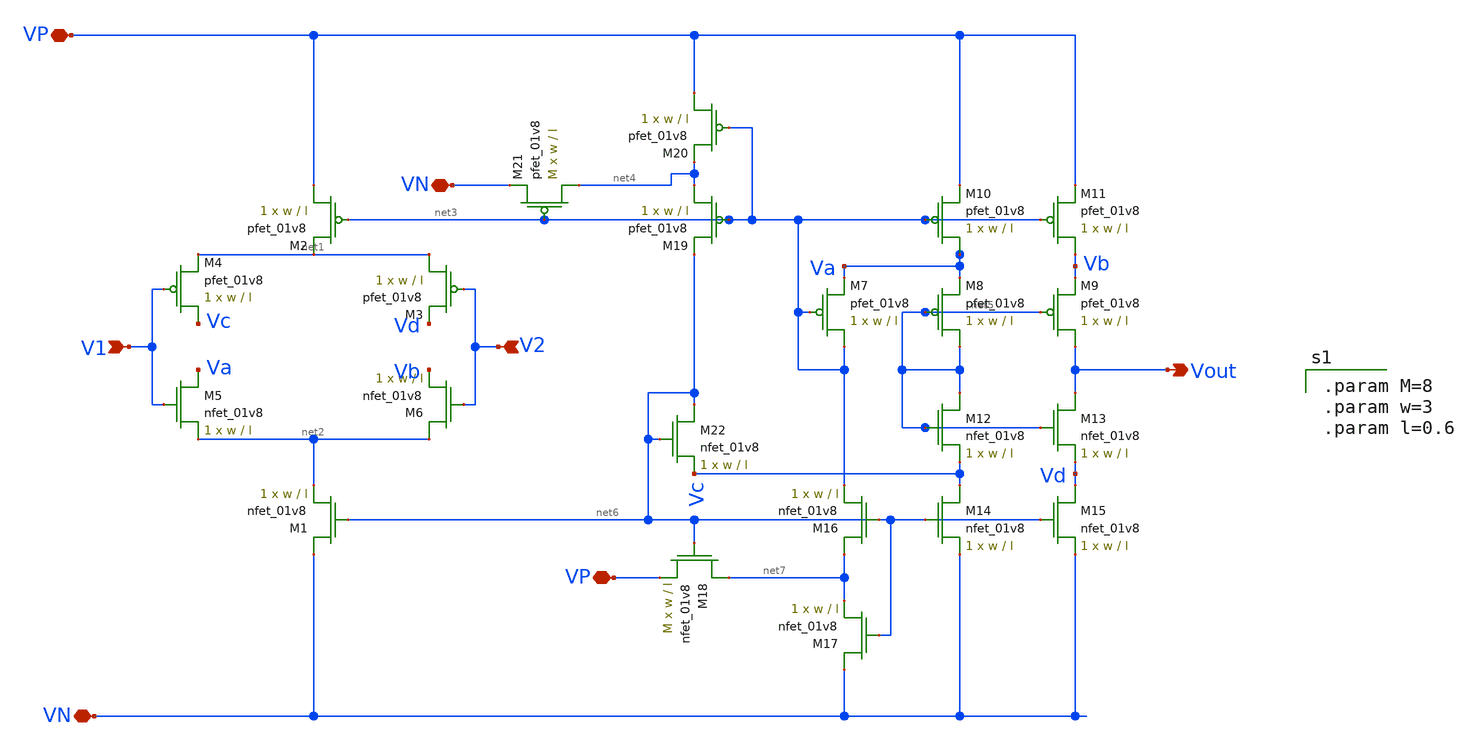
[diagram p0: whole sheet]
** sch_path: schematics/opamp.sch
**.subckt opamp V1 V2 Vout VP VN VP VN
*.ipin V1
*.ipin V2
*.opin Vout
*.iopin VP
*.iopin VN
*.iopin VP
*.iopin VN
XM1 VN net6 net2 GND sky130_fd_pr__nfet_01v8 L=l W=w nf=1 ad='int((nf+1)/2) * W/nf * 0.29' as='int((nf+2)/2) * W/nf * 0.29'
+ pd='2*int((nf+1)/2) * (W/nf + 0.29)' ps='2*int((nf+2)/2) * (W/nf + 0.29)' nrd='0.29 / W' nrs='0.29 / W'
+ sa=0 sb=0 sd=0 mult=1 m=1
XM2 VP net3 net1 VDD sky130_fd_pr__pfet_01v8 L=l W=w nf=1 ad='int((nf+1)/2) * W/nf * 0.29' as='int((nf+2)/2) * W/nf * 0.29'
+ pd='2*int((nf+1)/2) * (W/nf + 0.29)' ps='2*int((nf+2)/2) * (W/nf + 0.29)' nrd='0.29 / W' nrs='0.29 / W'
+ sa=0 sb=0 sd=0 mult=1 m=1
XM3 net1 V2 Vd VDD sky130_fd_pr__pfet_01v8 L=l W=w nf=1 ad='int((nf+1)/2) * W/nf * 0.29' as='int((nf+2)/2) * W/nf * 0.29'
+ pd='2*int((nf+1)/2) * (W/nf + 0.29)' ps='2*int((nf+2)/2) * (W/nf + 0.29)' nrd='0.29 / W' nrs='0.29 / W'
+ sa=0 sb=0 sd=0 mult=1 m=1
XM4 Vc V1 net1 VDD sky130_fd_pr__pfet_01v8 L=l W=w nf=1 ad='int((nf+1)/2) * W/nf * 0.29' as='int((nf+2)/2) * W/nf * 0.29'
+ pd='2*int((nf+1)/2) * (W/nf + 0.29)' ps='2*int((nf+2)/2) * (W/nf + 0.29)' nrd='0.29 / W' nrs='0.29 / W'
+ sa=0 sb=0 sd=0 mult=1 m=1
XM5 Va V1 net2 GND sky130_fd_pr__nfet_01v8 L=l W=w nf=1 ad='int((nf+1)/2) * W/nf * 0.29' as='int((nf+2)/2) * W/nf * 0.29'
+ pd='2*int((nf+1)/2) * (W/nf + 0.29)' ps='2*int((nf+2)/2) * (W/nf + 0.29)' nrd='0.29 / W' nrs='0.29 / W'
+ sa=0 sb=0 sd=0 mult=1 m=1
XM6 net2 V2 Vb GND sky130_fd_pr__nfet_01v8 L=l W=w nf=1 ad='int((nf+1)/2) * W/nf * 0.29' as='int((nf+2)/2) * W/nf * 0.29'
+ pd='2*int((nf+1)/2) * (W/nf + 0.29)' ps='2*int((nf+2)/2) * (W/nf + 0.29)' nrd='0.29 / W' nrs='0.29 / W'
+ sa=0 sb=0 sd=0 mult=1 m=1
XM7 net3 net3 Va VDD sky130_fd_pr__pfet_01v8 L=l W=w nf=1 ad='int((nf+1)/2) * W/nf * 0.29' as='int((nf+2)/2) * W/nf * 0.29'
+ pd='2*int((nf+1)/2) * (W/nf + 0.29)' ps='2*int((nf+2)/2) * (W/nf + 0.29)' nrd='0.29 / W' nrs='0.29 / W'
+ sa=0 sb=0 sd=0 mult=1 m=1
XM8 net5 net5 Va VDD sky130_fd_pr__pfet_01v8 L=l W=w nf=1 ad='int((nf+1)/2) * W/nf * 0.29' as='int((nf+2)/2) * W/nf * 0.29'
+ pd='2*int((nf+1)/2) * (W/nf + 0.29)' ps='2*int((nf+2)/2) * (W/nf + 0.29)' nrd='0.29 / W' nrs='0.29 / W'
+ sa=0 sb=0 sd=0 mult=1 m=1
XM9 Vout net5 Vb VDD sky130_fd_pr__pfet_01v8 L=l W=w nf=1 ad='int((nf+1)/2) * W/nf * 0.29' as='int((nf+2)/2) * W/nf * 0.29'
+ pd='2*int((nf+1)/2) * (W/nf + 0.29)' ps='2*int((nf+2)/2) * (W/nf + 0.29)' nrd='0.29 / W' nrs='0.29 / W'
+ sa=0 sb=0 sd=0 mult=1 m=1
XM10 Va net3 VP VDD sky130_fd_pr__pfet_01v8 L=l W=w nf=1 ad='int((nf+1)/2) * W/nf * 0.29' as='int((nf+2)/2) * W/nf * 0.29'
+ pd='2*int((nf+1)/2) * (W/nf + 0.29)' ps='2*int((nf+2)/2) * (W/nf + 0.29)' nrd='0.29 / W' nrs='0.29 / W'
+ sa=0 sb=0 sd=0 mult=1 m=1
XM11 Vb net3 VP VDD sky130_fd_pr__pfet_01v8 L=l W=w nf=1 ad='int((nf+1)/2) * W/nf * 0.29' as='int((nf+2)/2) * W/nf * 0.29'
+ pd='2*int((nf+1)/2) * (W/nf + 0.29)' ps='2*int((nf+2)/2) * (W/nf + 0.29)' nrd='0.29 / W' nrs='0.29 / W'
+ sa=0 sb=0 sd=0 mult=1 m=1
XM12 net5 net5 Vc GND sky130_fd_pr__nfet_01v8 L=l W=w nf=1 ad='int((nf+1)/2) * W/nf * 0.29' as='int((nf+2)/2) * W/nf * 0.29'
+ pd='2*int((nf+1)/2) * (W/nf + 0.29)' ps='2*int((nf+2)/2) * (W/nf + 0.29)' nrd='0.29 / W' nrs='0.29 / W'
+ sa=0 sb=0 sd=0 mult=1 m=1
XM13 Vout net5 Vd GND sky130_fd_pr__nfet_01v8 L=l W=w nf=1 ad='int((nf+1)/2) * W/nf * 0.29' as='int((nf+2)/2) * W/nf * 0.29'
+ pd='2*int((nf+1)/2) * (W/nf + 0.29)' ps='2*int((nf+2)/2) * (W/nf + 0.29)' nrd='0.29 / W' nrs='0.29 / W'
+ sa=0 sb=0 sd=0 mult=1 m=1
XM14 Vc net6 VN GND sky130_fd_pr__nfet_01v8 L=l W=w nf=1 ad='int((nf+1)/2) * W/nf * 0.29' as='int((nf+2)/2) * W/nf * 0.29'
+ pd='2*int((nf+1)/2) * (W/nf + 0.29)' ps='2*int((nf+2)/2) * (W/nf + 0.29)' nrd='0.29 / W' nrs='0.29 / W'
+ sa=0 sb=0 sd=0 mult=1 m=1
XM15 Vd net6 VN GND sky130_fd_pr__nfet_01v8 L=l W=w nf=1 ad='int((nf+1)/2) * W/nf * 0.29' as='int((nf+2)/2) * W/nf * 0.29'
+ pd='2*int((nf+1)/2) * (W/nf + 0.29)' ps='2*int((nf+2)/2) * (W/nf + 0.29)' nrd='0.29 / W' nrs='0.29 / W'
+ sa=0 sb=0 sd=0 mult=1 m=1
XM16 net7 net6 net3 GND sky130_fd_pr__nfet_01v8 L=l W=w nf=1 ad='int((nf+1)/2) * W/nf * 0.29' as='int((nf+2)/2) * W/nf * 0.29'
+ pd='2*int((nf+1)/2) * (W/nf + 0.29)' ps='2*int((nf+2)/2) * (W/nf + 0.29)' nrd='0.29 / W' nrs='0.29 / W'
+ sa=0 sb=0 sd=0 mult=1 m=1
XM17 VN net6 net7 GND sky130_fd_pr__nfet_01v8 L=l W=w nf=1 ad='int((nf+1)/2) * W/nf * 0.29' as='int((nf+2)/2) * W/nf * 0.29'
+ pd='2*int((nf+1)/2) * (W/nf + 0.29)' ps='2*int((nf+2)/2) * (W/nf + 0.29)' nrd='0.29 / W' nrs='0.29 / W'
+ sa=0 sb=0 sd=0 mult=1 m=1
XM18 net7 net6 VP GND sky130_fd_pr__nfet_01v8 L=l W=w nf=1 ad='int((nf+1)/2) * W/nf * 0.29' as='int((nf+2)/2) * W/nf * 0.29'
+ pd='2*int((nf+1)/2) * (W/nf + 0.29)' ps='2*int((nf+2)/2) * (W/nf + 0.29)' nrd='0.29 / W' nrs='0.29 / W'
+ sa=0 sb=0 sd=0 mult=M m=M
XM19 net4 net3 net6 VDD sky130_fd_pr__pfet_01v8 L=l W=w nf=1 ad='int((nf+1)/2) * W/nf * 0.29' as='int((nf+2)/2) * W/nf * 0.29'
+ pd='2*int((nf+1)/2) * (W/nf + 0.29)' ps='2*int((nf+2)/2) * (W/nf + 0.29)' nrd='0.29 / W' nrs='0.29 / W'
+ sa=0 sb=0 sd=0 mult=1 m=1
XM20 VP net3 net4 VDD sky130_fd_pr__pfet_01v8 L=l W=w nf=1 ad='int((nf+1)/2) * W/nf * 0.29' as='int((nf+2)/2) * W/nf * 0.29'
+ pd='2*int((nf+1)/2) * (W/nf + 0.29)' ps='2*int((nf+2)/2) * (W/nf + 0.29)' nrd='0.29 / W' nrs='0.29 / W'
+ sa=0 sb=0 sd=0 mult=1 m=1
XM21 net4 net3 VN VDD sky130_fd_pr__pfet_01v8 L=l W=w nf=1 ad='int((nf+1)/2) * W/nf * 0.29' as='int((nf+2)/2) * W/nf * 0.29'
+ pd='2*int((nf+1)/2) * (W/nf + 0.29)' ps='2*int((nf+2)/2) * (W/nf + 0.29)' nrd='0.29 / W' nrs='0.29 / W'
+ sa=0 sb=0 sd=0 mult=M m=M
XM22 net6 net6 Vc GND sky130_fd_pr__nfet_01v8 L=l W=w nf=1 ad='int((nf+1)/2) * W/nf * 0.29' as='int((nf+2)/2) * W/nf * 0.29'
+ pd='2*int((nf+1)/2) * (W/nf + 0.29)' ps='2*int((nf+2)/2) * (W/nf + 0.29)' nrd='0.29 / W' nrs='0.29 / W'
+ sa=0 sb=0 sd=0 mult=1 m=1
**** begin user architecture code

.param M=8
.param w=3
.param l=0.6


**** end user architecture code
**.ends
.end
